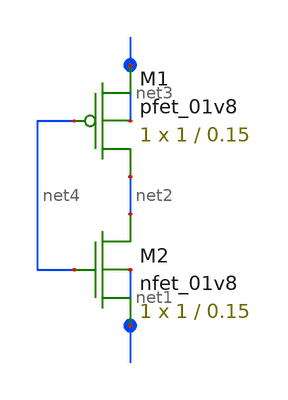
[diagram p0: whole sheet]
** sch_path: mp1/untitled-1.sch
**.subckt untitled-1
XM1 net2 net4 net3 net3 sky130_fd_pr__pfet_01v8 L=0.15 W=1 nf=1 ad='int((nf+1)/2) * W/nf * 0.29' as='int((nf+2)/2) * W/nf * 0.29'
+ pd='2*int((nf+1)/2) * (W/nf + 0.29)' ps='2*int((nf+2)/2) * (W/nf + 0.29)' nrd='0.29 / W' nrs='0.29 / W'
+ sa=0 sb=0 sd=0 mult=1 m=1
XM2 net2 net4 net1 net1 sky130_fd_pr__nfet_01v8 L=0.15 W=1 nf=1 ad='int((nf+1)/2) * W/nf * 0.29' as='int((nf+2)/2) * W/nf * 0.29'
+ pd='2*int((nf+1)/2) * (W/nf + 0.29)' ps='2*int((nf+2)/2) * (W/nf + 0.29)' nrd='0.29 / W' nrs='0.29 / W'
+ sa=0 sb=0 sd=0 mult=1 m=1
**.ends
.end
